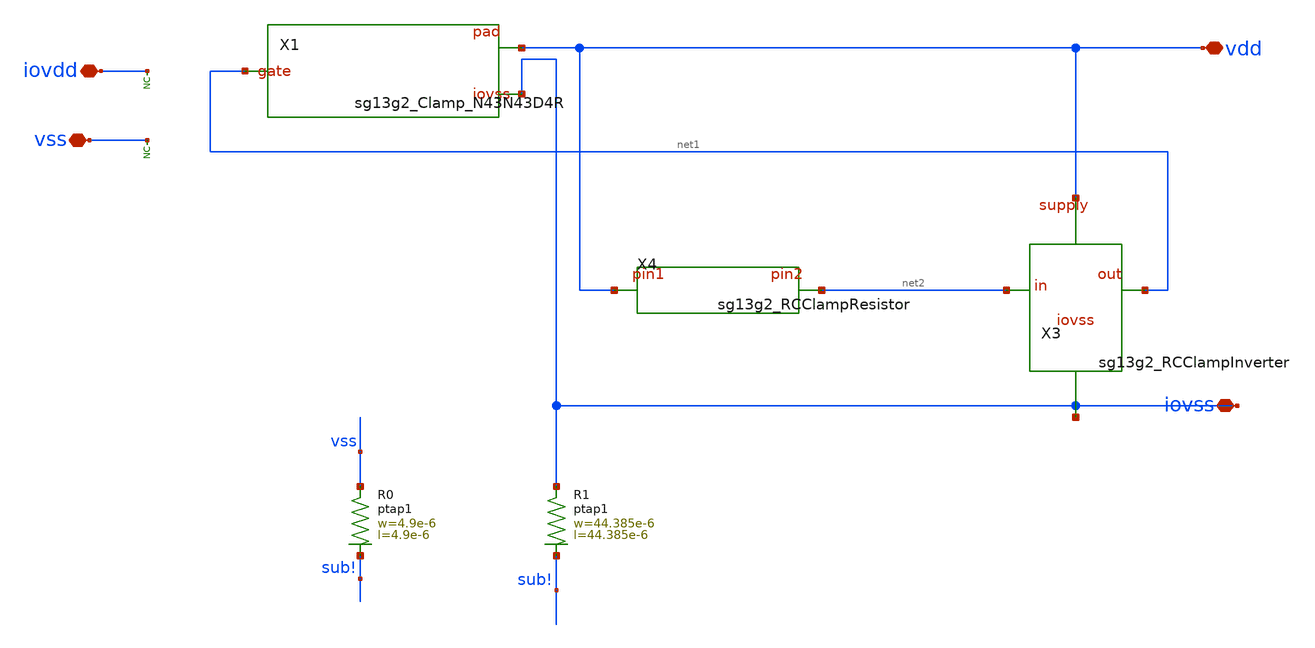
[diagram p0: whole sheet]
** sch_path: ihp-sg13g2/libs.ref/sg13g2_io/sch/xschem/sg13g2_IOPadVdd.sch
**.subckt sg13g2_IOPadVdd iovss iovdd vss vdd
*.iopin iovss
*.iopin iovdd
*.iopin vss
*.iopin vdd
* noconn iovdd
* noconn vss
X1 net1 iovss vdd sg13g2_Clamp_N43N43D4R
X3 vdd net1 net2 iovss sg13g2_RCClampInverter
X4 net2 vdd sg13g2_RCClampResistor
XR0 vss sub! ptap1 R=22.47 w=4.9e-6 l=4.9e-6
XR1 iovss sub! ptap1 R=456.3m w=44.385e-6 l=44.385e-6
**.ends
.end
